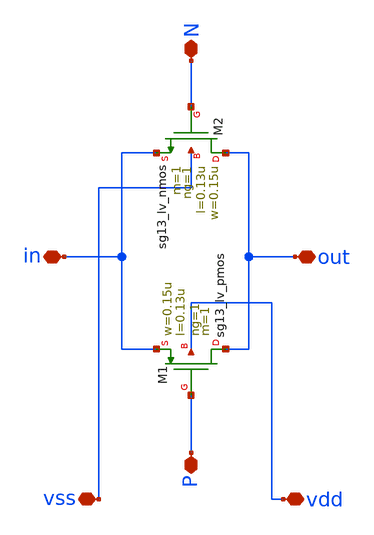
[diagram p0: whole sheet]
** sch_path: design/blocks/interruptor/interruptor.sch
**.subckt interruptor N in out vdd vss P
*.iopin N
*.iopin in
*.iopin out
*.iopin vdd
*.iopin vss
*.iopin P
XM1 out P in vdd sg13_lv_pmos w=0.15u l=0.13u ng=1 m=1 mm_ok=1
XM2 out N in vss sg13_lv_nmos w=0.15u l=0.13u ng=1 m=1 mm_ok=1
**.ends
.end
